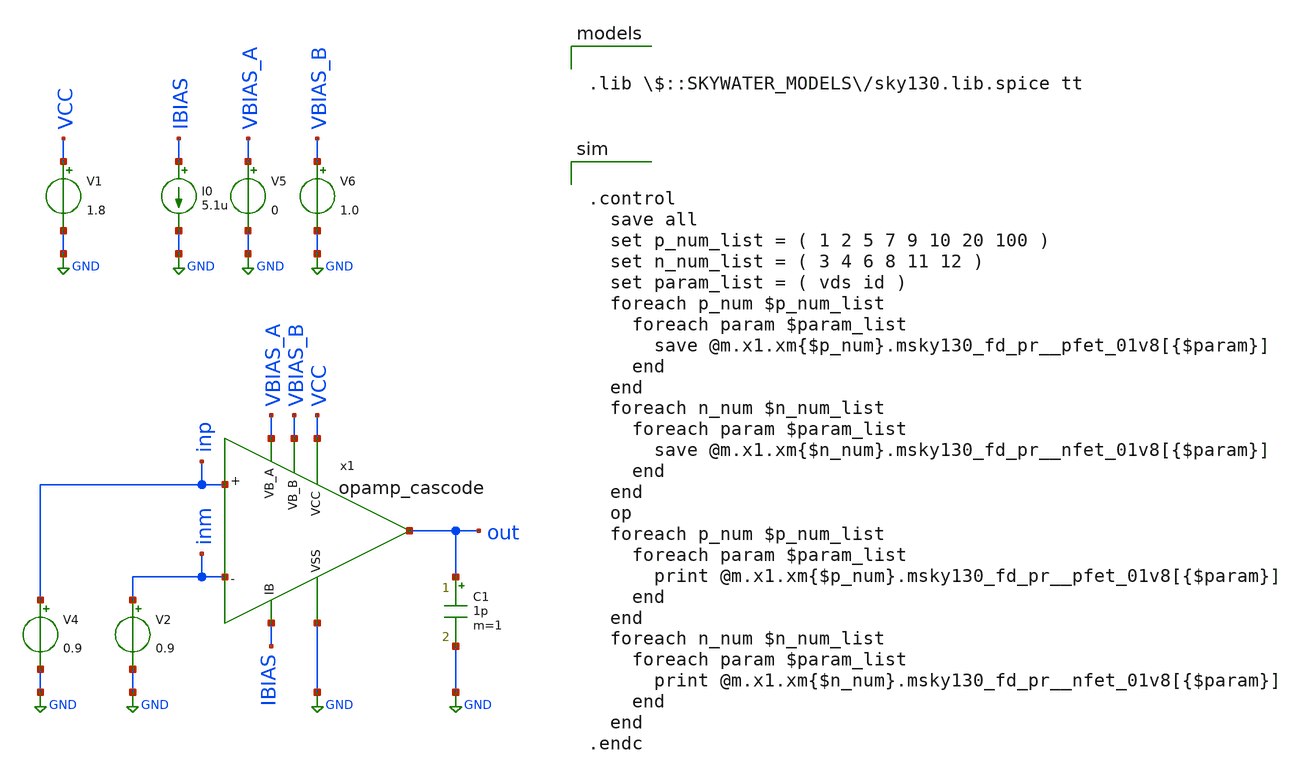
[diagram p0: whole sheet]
** sch_path: opamp_cascode_op_point.sch
**.subckt opamp_cascode_op_point
V1 VCC GND 1.8
V4 inp GND 0.9
V2 inm GND 0.9
C1 out GND 1p m=1
x1 VCC GND VBIAS_B inp inm out IBIAS VBIAS_A opamp_cascode
V5 VBIAS_A GND 0
V6 VBIAS_B GND 1.0
I0 IBIAS GND 5.1u
**** begin user architecture code


.control
  save all
  set p_num_list = ( 1 2 5 7 9 10 20 100 )
  set n_num_list = ( 3 4 6 8 11 12 )
  set param_list = ( vds id )
  foreach p_num $p_num_list
    foreach param $param_list
      save @m.x1.xm{$p_num}.msky130_fd_pr__pfet_01v8[{$param}]
    end
  end
  foreach n_num $n_num_list
    foreach param $param_list
      save @m.x1.xm{$n_num}.msky130_fd_pr__nfet_01v8[{$param}]
    end
  end
  op
  foreach p_num $p_num_list
    foreach param $param_list
      print @m.x1.xm{$p_num}.msky130_fd_pr__pfet_01v8[{$param}]
    end
  end
  foreach n_num $n_num_list
    foreach param $param_list
      print @m.x1.xm{$n_num}.msky130_fd_pr__nfet_01v8[{$param}]
    end
  end
.endc



.lib $::SKYWATER_MODELS/sky130.lib.spice tt

**** end user architecture code
**.ends

* expanding   symbol:  /home/zwierzak/projects/SKY130_OpAmp_GIT/opamp_cascode.sym # of pins=8
** sym_path: 03_Layout/opamp_cascode.sym
** sch_path: 03_Layout/opamp_cascode.sch
.subckt opamp_cascode VCC VSS VB_B IN_P IN_M OUT IB VB_A
*.ipin IN_P
*.ipin IN_M
*.ipin VCC
*.ipin VSS
*.opin OUT
*.ipin VB_A
*.ipin VB_B
*.ipin IB
XM100_3 IB IB VCC VCC sky130_fd_pr__pfet_01v8 L=3 W=5 nf=1 ad='int((nf+1)/2) * W/nf * 0.29' as='int((nf+2)/2) * W/nf * 0.29'
+ pd='2*int((nf+1)/2) * (W/nf + 0.29)' ps='2*int((nf+2)/2) * (W/nf + 0.29)' nrd='0.29 / W' nrs='0.29 / W'
+ sa=0 sb=0 sd=0 mult=2 m=2
XM10 OUT VB_A m9m10 VCC sky130_fd_pr__pfet_01v8 L=5 W=5 nf=1 ad='int((nf+1)/2) * W/nf * 0.29' as='int((nf+2)/2) * W/nf * 0.29'
+ pd='2*int((nf+1)/2) * (W/nf + 0.29)' ps='2*int((nf+2)/2) * (W/nf + 0.29)' nrd='0.29 / W' nrs='0.29 / W'
+ sa=0 sb=0 sd=0 mult=15 m=15
XM2 bias1 VB_A m1m2 VCC sky130_fd_pr__pfet_01v8 L=5 W=5 nf=1 ad='int((nf+1)/2) * W/nf * 0.29' as='int((nf+2)/2) * W/nf * 0.29'
+ pd='2*int((nf+1)/2) * (W/nf + 0.29)' ps='2*int((nf+2)/2) * (W/nf + 0.29)' nrd='0.29 / W' nrs='0.29 / W'
+ sa=0 sb=0 sd=0 mult=15 m=15
XM5 bias3 IN_M m100m5 VCC sky130_fd_pr__pfet_01v8 L=0.18 W=5 nf=1 ad='int((nf+1)/2) * W/nf * 0.29' as='int((nf+2)/2) * W/nf * 0.29'
+ pd='2*int((nf+1)/2) * (W/nf + 0.29)' ps='2*int((nf+2)/2) * (W/nf + 0.29)' nrd='0.29 / W' nrs='0.29 / W'
+ sa=0 sb=0 sd=0 mult=15 m=15
XM7 bias21 IN_P m100m5 VCC sky130_fd_pr__pfet_01v8 L=0.18 W=5 nf=1 ad='int((nf+1)/2) * W/nf * 0.29' as='int((nf+2)/2) * W/nf * 0.29'
+ pd='2*int((nf+1)/2) * (W/nf + 0.29)' ps='2*int((nf+2)/2) * (W/nf + 0.29)' nrd='0.29 / W' nrs='0.29 / W'
+ sa=0 sb=0 sd=0 mult=15 m=15
XM6 bias3 bias3 VSS VSS sky130_fd_pr__nfet_01v8 L=1 W=1.25 nf=1 ad='int((nf+1)/2) * W/nf * 0.29' as='int((nf+2)/2) * W/nf * 0.29'
+ pd='2*int((nf+1)/2) * (W/nf + 0.29)' ps='2*int((nf+2)/2) * (W/nf + 0.29)' nrd='0.29 / W' nrs='0.29 / W'
+ sa=0 sb=0 sd=0 mult=1 m=1
XM8 bias21 bias21 VSS VSS sky130_fd_pr__nfet_01v8 L=1 W=1.25 nf=1 ad='int((nf+1)/2) * W/nf * 0.29' as='int((nf+2)/2) * W/nf * 0.29'
+ pd='2*int((nf+1)/2) * (W/nf + 0.29)' ps='2*int((nf+2)/2) * (W/nf + 0.29)' nrd='0.29 / W' nrs='0.29 / W'
+ sa=0 sb=0 sd=0 mult=1 m=1
XM12 m11m12 bias21 VSS VSS sky130_fd_pr__nfet_01v8 L=1 W=5 nf=1 ad='int((nf+1)/2) * W/nf * 0.29' as='int((nf+2)/2) * W/nf * 0.29'
+ pd='2*int((nf+1)/2) * (W/nf + 0.29)' ps='2*int((nf+2)/2) * (W/nf + 0.29)' nrd='0.29 / W' nrs='0.29 / W'
+ sa=0 sb=0 sd=0 mult=1 m=1
XM11 OUT VB_B m11m12 VSS sky130_fd_pr__nfet_01v8 L=5 W=5 nf=1 ad='int((nf+1)/2) * W/nf * 0.29' as='int((nf+2)/2) * W/nf * 0.29'
+ pd='2*int((nf+1)/2) * (W/nf + 0.29)' ps='2*int((nf+2)/2) * (W/nf + 0.29)' nrd='0.29 / W' nrs='0.29 / W'
+ sa=0 sb=0 sd=0 mult=15 m=15
XM3 bias1 VB_B m3m4 VSS sky130_fd_pr__nfet_01v8 L=5 W=5 nf=1 ad='int((nf+1)/2) * W/nf * 0.29' as='int((nf+2)/2) * W/nf * 0.29'
+ pd='2*int((nf+1)/2) * (W/nf + 0.29)' ps='2*int((nf+2)/2) * (W/nf + 0.29)' nrd='0.29 / W' nrs='0.29 / W'
+ sa=0 sb=0 sd=0 mult=15 m=15
XM100_1 m100m5 IB VCC VCC sky130_fd_pr__pfet_01v8 L=3 W=5 nf=1 ad='int((nf+1)/2) * W/nf * 0.29' as='int((nf+2)/2) * W/nf * 0.29'
+ pd='2*int((nf+1)/2) * (W/nf + 0.29)' ps='2*int((nf+2)/2) * (W/nf + 0.29)' nrd='0.29 / W' nrs='0.29 / W'
+ sa=0 sb=0 sd=0 mult=3 m=3
XM5_1 bias3 IN_M m100m5 VCC sky130_fd_pr__pfet_01v8 L=0.18 W=5 nf=1 ad='int((nf+1)/2) * W/nf * 0.29'
+ as='int((nf+2)/2) * W/nf * 0.29' pd='2*int((nf+1)/2) * (W/nf + 0.29)' ps='2*int((nf+2)/2) * (W/nf + 0.29)'
+ nrd='0.29 / W' nrs='0.29 / W' sa=0 sb=0 sd=0 mult=15 m=15
XM7_1 bias21 IN_P m100m5 VCC sky130_fd_pr__pfet_01v8 L=0.18 W=5 nf=1 ad='int((nf+1)/2) * W/nf * 0.29'
+ as='int((nf+2)/2) * W/nf * 0.29' pd='2*int((nf+1)/2) * (W/nf + 0.29)' ps='2*int((nf+2)/2) * (W/nf + 0.29)'
+ nrd='0.29 / W' nrs='0.29 / W' sa=0 sb=0 sd=0 mult=15 m=15
XM9 m9m10 bias1 VCC VCC sky130_fd_pr__pfet_01v8 L=15 W=5 nf=1 ad='int((nf+1)/2) * W/nf * 0.29' as='int((nf+2)/2) * W/nf * 0.29'
+ pd='2*int((nf+1)/2) * (W/nf + 0.29)' ps='2*int((nf+2)/2) * (W/nf + 0.29)' nrd='0.29 / W' nrs='0.29 / W'
+ sa=0 sb=0 sd=0 mult=100 m=100
XM9_1 m9m10 bias1 VCC VCC sky130_fd_pr__pfet_01v8 L=15 W=5 nf=1 ad='int((nf+1)/2) * W/nf * 0.29' as='int((nf+2)/2) * W/nf * 0.29'
+ pd='2*int((nf+1)/2) * (W/nf + 0.29)' ps='2*int((nf+2)/2) * (W/nf + 0.29)' nrd='0.29 / W' nrs='0.29 / W'
+ sa=0 sb=0 sd=0 mult=100 m=100
XM9_2 m9m10 bias1 VCC VCC sky130_fd_pr__pfet_01v8 L=15 W=5 nf=1 ad='int((nf+1)/2) * W/nf * 0.29' as='int((nf+2)/2) * W/nf * 0.29'
+ pd='2*int((nf+1)/2) * (W/nf + 0.29)' ps='2*int((nf+2)/2) * (W/nf + 0.29)' nrd='0.29 / W' nrs='0.29 / W'
+ sa=0 sb=0 sd=0 mult=100 m=100
XM9_3 m9m10 bias1 VCC VCC sky130_fd_pr__pfet_01v8 L=15 W=5 nf=1 ad='int((nf+1)/2) * W/nf * 0.29' as='int((nf+2)/2) * W/nf * 0.29'
+ pd='2*int((nf+1)/2) * (W/nf + 0.29)' ps='2*int((nf+2)/2) * (W/nf + 0.29)' nrd='0.29 / W' nrs='0.29 / W'
+ sa=0 sb=0 sd=0 mult=100 m=100
XM9_4 m9m10 bias1 VCC VCC sky130_fd_pr__pfet_01v8 L=15 W=5 nf=1 ad='int((nf+1)/2) * W/nf * 0.29' as='int((nf+2)/2) * W/nf * 0.29'
+ pd='2*int((nf+1)/2) * (W/nf + 0.29)' ps='2*int((nf+2)/2) * (W/nf + 0.29)' nrd='0.29 / W' nrs='0.29 / W'
+ sa=0 sb=0 sd=0 mult=100 m=100
XM1 m1m2 bias1 VCC VCC sky130_fd_pr__pfet_01v8 L=15 W=5 nf=1 ad='int((nf+1)/2) * W/nf * 0.29' as='int((nf+2)/2) * W/nf * 0.29'
+ pd='2*int((nf+1)/2) * (W/nf + 0.29)' ps='2*int((nf+2)/2) * (W/nf + 0.29)' nrd='0.29 / W' nrs='0.29 / W'
+ sa=0 sb=0 sd=0 mult=100 m=100
XM1_1 m1m2 bias1 VCC VCC sky130_fd_pr__pfet_01v8 L=15 W=5 nf=1 ad='int((nf+1)/2) * W/nf * 0.29' as='int((nf+2)/2) * W/nf * 0.29'
+ pd='2*int((nf+1)/2) * (W/nf + 0.29)' ps='2*int((nf+2)/2) * (W/nf + 0.29)' nrd='0.29 / W' nrs='0.29 / W'
+ sa=0 sb=0 sd=0 mult=100 m=100
XM1_2 m1m2 bias1 VCC VCC sky130_fd_pr__pfet_01v8 L=15 W=5 nf=1 ad='int((nf+1)/2) * W/nf * 0.29' as='int((nf+2)/2) * W/nf * 0.29'
+ pd='2*int((nf+1)/2) * (W/nf + 0.29)' ps='2*int((nf+2)/2) * (W/nf + 0.29)' nrd='0.29 / W' nrs='0.29 / W'
+ sa=0 sb=0 sd=0 mult=100 m=100
XM1_3 m1m2 bias1 VCC VCC sky130_fd_pr__pfet_01v8 L=15 W=5 nf=1 ad='int((nf+1)/2) * W/nf * 0.29' as='int((nf+2)/2) * W/nf * 0.29'
+ pd='2*int((nf+1)/2) * (W/nf + 0.29)' ps='2*int((nf+2)/2) * (W/nf + 0.29)' nrd='0.29 / W' nrs='0.29 / W'
+ sa=0 sb=0 sd=0 mult=100 m=100
XM1_4 m1m2 bias1 VCC VCC sky130_fd_pr__pfet_01v8 L=15 W=5 nf=1 ad='int((nf+1)/2) * W/nf * 0.29' as='int((nf+2)/2) * W/nf * 0.29'
+ pd='2*int((nf+1)/2) * (W/nf + 0.29)' ps='2*int((nf+2)/2) * (W/nf + 0.29)' nrd='0.29 / W' nrs='0.29 / W'
+ sa=0 sb=0 sd=0 mult=100 m=100
XM100_2 m100m5 IB VCC VCC sky130_fd_pr__pfet_01v8 L=3 W=5 nf=1 ad='int((nf+1)/2) * W/nf * 0.29' as='int((nf+2)/2) * W/nf * 0.29'
+ pd='2*int((nf+1)/2) * (W/nf + 0.29)' ps='2*int((nf+2)/2) * (W/nf + 0.29)' nrd='0.29 / W' nrs='0.29 / W'
+ sa=0 sb=0 sd=0 mult=3 m=3
XM10_1 OUT VB_A m9m10 VCC sky130_fd_pr__pfet_01v8 L=5 W=5 nf=1 ad='int((nf+1)/2) * W/nf * 0.29' as='int((nf+2)/2) * W/nf * 0.29'
+ pd='2*int((nf+1)/2) * (W/nf + 0.29)' ps='2*int((nf+2)/2) * (W/nf + 0.29)' nrd='0.29 / W' nrs='0.29 / W'
+ sa=0 sb=0 sd=0 mult=15 m=15
XM2_1 bias1 VB_A m1m2 VCC sky130_fd_pr__pfet_01v8 L=5 W=5 nf=1 ad='int((nf+1)/2) * W/nf * 0.29' as='int((nf+2)/2) * W/nf * 0.29'
+ pd='2*int((nf+1)/2) * (W/nf + 0.29)' ps='2*int((nf+2)/2) * (W/nf + 0.29)' nrd='0.29 / W' nrs='0.29 / W'
+ sa=0 sb=0 sd=0 mult=15 m=15
XM3_1 bias1 VB_B m3m4 VSS sky130_fd_pr__nfet_01v8 L=5 W=5 nf=1 ad='int((nf+1)/2) * W/nf * 0.29' as='int((nf+2)/2) * W/nf * 0.29'
+ pd='2*int((nf+1)/2) * (W/nf + 0.29)' ps='2*int((nf+2)/2) * (W/nf + 0.29)' nrd='0.29 / W' nrs='0.29 / W'
+ sa=0 sb=0 sd=0 mult=15 m=15
XM11_1 OUT VB_B m11m12 VSS sky130_fd_pr__nfet_01v8 L=5 W=5 nf=1 ad='int((nf+1)/2) * W/nf * 0.29' as='int((nf+2)/2) * W/nf * 0.29'
+ pd='2*int((nf+1)/2) * (W/nf + 0.29)' ps='2*int((nf+2)/2) * (W/nf + 0.29)' nrd='0.29 / W' nrs='0.29 / W'
+ sa=0 sb=0 sd=0 mult=15 m=15
XM4 m3m4 bias3 VSS VSS sky130_fd_pr__nfet_01v8 L=1 W=5 nf=1 ad='int((nf+1)/2) * W/nf * 0.29' as='int((nf+2)/2) * W/nf * 0.29'
+ pd='2*int((nf+1)/2) * (W/nf + 0.29)' ps='2*int((nf+2)/2) * (W/nf + 0.29)' nrd='0.29 / W' nrs='0.29 / W'
+ sa=0 sb=0 sd=0 mult=1 m=1
XM6_1 bias3 bias3 VSS VSS sky130_fd_pr__nfet_01v8 L=1 W=1.25 nf=1 ad='int((nf+1)/2) * W/nf * 0.29' as='int((nf+2)/2) * W/nf * 0.29'
+ pd='2*int((nf+1)/2) * (W/nf + 0.29)' ps='2*int((nf+2)/2) * (W/nf + 0.29)' nrd='0.29 / W' nrs='0.29 / W'
+ sa=0 sb=0 sd=0 mult=1 m=1
XM8_1 bias21 bias21 VSS VSS sky130_fd_pr__nfet_01v8 L=1 W=1.25 nf=1 ad='int((nf+1)/2) * W/nf * 0.29'
+ as='int((nf+2)/2) * W/nf * 0.29' pd='2*int((nf+1)/2) * (W/nf + 0.29)' ps='2*int((nf+2)/2) * (W/nf + 0.29)'
+ nrd='0.29 / W' nrs='0.29 / W' sa=0 sb=0 sd=0 mult=1 m=1
XM6_2 bias3 bias3 VSS VSS sky130_fd_pr__nfet_01v8 L=1 W=1.25 nf=1 ad='int((nf+1)/2) * W/nf * 0.29' as='int((nf+2)/2) * W/nf * 0.29'
+ pd='2*int((nf+1)/2) * (W/nf + 0.29)' ps='2*int((nf+2)/2) * (W/nf + 0.29)' nrd='0.29 / W' nrs='0.29 / W'
+ sa=0 sb=0 sd=0 mult=1 m=1
XM6_3 bias3 bias3 VSS VSS sky130_fd_pr__nfet_01v8 L=1 W=1.25 nf=1 ad='int((nf+1)/2) * W/nf * 0.29' as='int((nf+2)/2) * W/nf * 0.29'
+ pd='2*int((nf+1)/2) * (W/nf + 0.29)' ps='2*int((nf+2)/2) * (W/nf + 0.29)' nrd='0.29 / W' nrs='0.29 / W'
+ sa=0 sb=0 sd=0 mult=1 m=1
XM9_dummy_1 dummy_9 bias1 dummy_9 VCC sky130_fd_pr__pfet_01v8 L=15 W=5 nf=1 ad='int((nf+1)/2) * W/nf * 0.29'
+ as='int((nf+2)/2) * W/nf * 0.29' pd='2*int((nf+1)/2) * (W/nf + 0.29)' ps='2*int((nf+2)/2) * (W/nf + 0.29)'
+ nrd='0.29 / W' nrs='0.29 / W' sa=0 sb=0 sd=0 mult=102 m=102
XM9_dummy_2 dummy_9 bias1 dummy_9 VCC sky130_fd_pr__pfet_01v8 L=15 W=5 nf=1 ad='int((nf+1)/2) * W/nf * 0.29'
+ as='int((nf+2)/2) * W/nf * 0.29' pd='2*int((nf+1)/2) * (W/nf + 0.29)' ps='2*int((nf+2)/2) * (W/nf + 0.29)'
+ nrd='0.29 / W' nrs='0.29 / W' sa=0 sb=0 sd=0 mult=102 m=102
XM9_dummy_3 dummy_9 bias1 dummy_9 VCC sky130_fd_pr__pfet_01v8 L=15 W=5 nf=1 ad='int((nf+1)/2) * W/nf * 0.29'
+ as='int((nf+2)/2) * W/nf * 0.29' pd='2*int((nf+1)/2) * (W/nf + 0.29)' ps='2*int((nf+2)/2) * (W/nf + 0.29)'
+ nrd='0.29 / W' nrs='0.29 / W' sa=0 sb=0 sd=0 mult=1 m=1
XM9_dummy_4 dummy_9 bias1 dummy_9 VCC sky130_fd_pr__pfet_01v8 L=15 W=5 nf=1 ad='int((nf+1)/2) * W/nf * 0.29'
+ as='int((nf+2)/2) * W/nf * 0.29' pd='2*int((nf+1)/2) * (W/nf + 0.29)' ps='2*int((nf+2)/2) * (W/nf + 0.29)'
+ nrd='0.29 / W' nrs='0.29 / W' sa=0 sb=0 sd=0 mult=1 m=1
XM9_dummy_5 dummy_9 bias1 dummy_9 VCC sky130_fd_pr__pfet_01v8 L=15 W=5 nf=1 ad='int((nf+1)/2) * W/nf * 0.29'
+ as='int((nf+2)/2) * W/nf * 0.29' pd='2*int((nf+1)/2) * (W/nf + 0.29)' ps='2*int((nf+2)/2) * (W/nf + 0.29)'
+ nrd='0.29 / W' nrs='0.29 / W' sa=0 sb=0 sd=0 mult=1 m=1
XM9_dummy_6 dummy_9 bias1 dummy_9 VCC sky130_fd_pr__pfet_01v8 L=15 W=5 nf=1 ad='int((nf+1)/2) * W/nf * 0.29'
+ as='int((nf+2)/2) * W/nf * 0.29' pd='2*int((nf+1)/2) * (W/nf + 0.29)' ps='2*int((nf+2)/2) * (W/nf + 0.29)'
+ nrd='0.29 / W' nrs='0.29 / W' sa=0 sb=0 sd=0 mult=1 m=1
XM9_dummy_7 dummy_9 bias1 dummy_9 VCC sky130_fd_pr__pfet_01v8 L=15 W=5 nf=1 ad='int((nf+1)/2) * W/nf * 0.29'
+ as='int((nf+2)/2) * W/nf * 0.29' pd='2*int((nf+1)/2) * (W/nf + 0.29)' ps='2*int((nf+2)/2) * (W/nf + 0.29)'
+ nrd='0.29 / W' nrs='0.29 / W' sa=0 sb=0 sd=0 mult=1 m=1
XM9_dummy_8 dummy_9 bias1 dummy_9 VCC sky130_fd_pr__pfet_01v8 L=15 W=5 nf=1 ad='int((nf+1)/2) * W/nf * 0.29'
+ as='int((nf+2)/2) * W/nf * 0.29' pd='2*int((nf+1)/2) * (W/nf + 0.29)' ps='2*int((nf+2)/2) * (W/nf + 0.29)'
+ nrd='0.29 / W' nrs='0.29 / W' sa=0 sb=0 sd=0 mult=1 m=1
XM9_dummy_9 dummy_9 bias1 dummy_9 VCC sky130_fd_pr__pfet_01v8 L=15 W=5 nf=1 ad='int((nf+1)/2) * W/nf * 0.29'
+ as='int((nf+2)/2) * W/nf * 0.29' pd='2*int((nf+1)/2) * (W/nf + 0.29)' ps='2*int((nf+2)/2) * (W/nf + 0.29)'
+ nrd='0.29 / W' nrs='0.29 / W' sa=0 sb=0 sd=0 mult=1 m=1
XM9_dummy_10 dummy_9 bias1 dummy_9 VCC sky130_fd_pr__pfet_01v8 L=15 W=5 nf=1 ad='int((nf+1)/2) * W/nf * 0.29'
+ as='int((nf+2)/2) * W/nf * 0.29' pd='2*int((nf+1)/2) * (W/nf + 0.29)' ps='2*int((nf+2)/2) * (W/nf + 0.29)'
+ nrd='0.29 / W' nrs='0.29 / W' sa=0 sb=0 sd=0 mult=1 m=1
XM9_dummy_11 dummy_9 bias1 dummy_9 VCC sky130_fd_pr__pfet_01v8 L=15 W=5 nf=1 ad='int((nf+1)/2) * W/nf * 0.29'
+ as='int((nf+2)/2) * W/nf * 0.29' pd='2*int((nf+1)/2) * (W/nf + 0.29)' ps='2*int((nf+2)/2) * (W/nf + 0.29)'
+ nrd='0.29 / W' nrs='0.29 / W' sa=0 sb=0 sd=0 mult=1 m=1
XM9_dummy_12 dummy_9 bias1 dummy_9 VCC sky130_fd_pr__pfet_01v8 L=15 W=5 nf=1 ad='int((nf+1)/2) * W/nf * 0.29'
+ as='int((nf+2)/2) * W/nf * 0.29' pd='2*int((nf+1)/2) * (W/nf + 0.29)' ps='2*int((nf+2)/2) * (W/nf + 0.29)'
+ nrd='0.29 / W' nrs='0.29 / W' sa=0 sb=0 sd=0 mult=1 m=1
XM100_dummy_1 dummy_100 IB dummy_100 VCC sky130_fd_pr__pfet_01v8 L=3 W=5 nf=1 ad='int((nf+1)/2) * W/nf * 0.29'
+ as='int((nf+2)/2) * W/nf * 0.29' pd='2*int((nf+1)/2) * (W/nf + 0.29)' ps='2*int((nf+2)/2) * (W/nf + 0.29)'
+ nrd='0.29 / W' nrs='0.29 / W' sa=0 sb=0 sd=0 mult=5 m=5
XM100_dummy_2 dummy_100 IB dummy_100 VCC sky130_fd_pr__pfet_01v8 L=3 W=5 nf=1 ad='int((nf+1)/2) * W/nf * 0.29'
+ as='int((nf+2)/2) * W/nf * 0.29' pd='2*int((nf+1)/2) * (W/nf + 0.29)' ps='2*int((nf+2)/2) * (W/nf + 0.29)'
+ nrd='0.29 / W' nrs='0.29 / W' sa=0 sb=0 sd=0 mult=5 m=5
XM100_dummy_3 dummy_100 IB dummy_100 VCC sky130_fd_pr__pfet_01v8 L=3 W=5 nf=1 ad='int((nf+1)/2) * W/nf * 0.29'
+ as='int((nf+2)/2) * W/nf * 0.29' pd='2*int((nf+1)/2) * (W/nf + 0.29)' ps='2*int((nf+2)/2) * (W/nf + 0.29)'
+ nrd='0.29 / W' nrs='0.29 / W' sa=0 sb=0 sd=0 mult=2 m=2
XM100_dummy_4 dummy_100 IB dummy_100 VCC sky130_fd_pr__pfet_01v8 L=3 W=5 nf=1 ad='int((nf+1)/2) * W/nf * 0.29'
+ as='int((nf+2)/2) * W/nf * 0.29' pd='2*int((nf+1)/2) * (W/nf + 0.29)' ps='2*int((nf+2)/2) * (W/nf + 0.29)'
+ nrd='0.29 / W' nrs='0.29 / W' sa=0 sb=0 sd=0 mult=2 m=2
XM100_dummy_5 dummy_100 IB dummy_100 VCC sky130_fd_pr__pfet_01v8 L=3 W=5 nf=1 ad='int((nf+1)/2) * W/nf * 0.29'
+ as='int((nf+2)/2) * W/nf * 0.29' pd='2*int((nf+1)/2) * (W/nf + 0.29)' ps='2*int((nf+2)/2) * (W/nf + 0.29)'
+ nrd='0.29 / W' nrs='0.29 / W' sa=0 sb=0 sd=0 mult=1 m=1
XM100_dummy_6 dummy_100 IB dummy_100 VCC sky130_fd_pr__pfet_01v8 L=3 W=5 nf=1 ad='int((nf+1)/2) * W/nf * 0.29'
+ as='int((nf+2)/2) * W/nf * 0.29' pd='2*int((nf+1)/2) * (W/nf + 0.29)' ps='2*int((nf+2)/2) * (W/nf + 0.29)'
+ nrd='0.29 / W' nrs='0.29 / W' sa=0 sb=0 sd=0 mult=1 m=1
XM100_dummy_7 dummy_100 IB dummy_100 VCC sky130_fd_pr__pfet_01v8 L=3 W=5 nf=1 ad='int((nf+1)/2) * W/nf * 0.29'
+ as='int((nf+2)/2) * W/nf * 0.29' pd='2*int((nf+1)/2) * (W/nf + 0.29)' ps='2*int((nf+2)/2) * (W/nf + 0.29)'
+ nrd='0.29 / W' nrs='0.29 / W' sa=0 sb=0 sd=0 mult=1 m=1
XM100_dummy_8 dummy_100 IB dummy_100 VCC sky130_fd_pr__pfet_01v8 L=3 W=5 nf=1 ad='int((nf+1)/2) * W/nf * 0.29'
+ as='int((nf+2)/2) * W/nf * 0.29' pd='2*int((nf+1)/2) * (W/nf + 0.29)' ps='2*int((nf+2)/2) * (W/nf + 0.29)'
+ nrd='0.29 / W' nrs='0.29 / W' sa=0 sb=0 sd=0 mult=1 m=1
XM100_dummy_9 dummy_100 IB dummy_100 VCC sky130_fd_pr__pfet_01v8 L=3 W=5 nf=1 ad='int((nf+1)/2) * W/nf * 0.29'
+ as='int((nf+2)/2) * W/nf * 0.29' pd='2*int((nf+1)/2) * (W/nf + 0.29)' ps='2*int((nf+2)/2) * (W/nf + 0.29)'
+ nrd='0.29 / W' nrs='0.29 / W' sa=0 sb=0 sd=0 mult=1 m=1
XM100_dummy_10 dummy_100 IB dummy_100 VCC sky130_fd_pr__pfet_01v8 L=3 W=5 nf=1 ad='int((nf+1)/2) * W/nf * 0.29'
+ as='int((nf+2)/2) * W/nf * 0.29' pd='2*int((nf+1)/2) * (W/nf + 0.29)' ps='2*int((nf+2)/2) * (W/nf + 0.29)'
+ nrd='0.29 / W' nrs='0.29 / W' sa=0 sb=0 sd=0 mult=1 m=1
XM2_dummy_1 dummy_2 VB_A dummy_2 VCC sky130_fd_pr__pfet_01v8 L=5 W=5 nf=1 ad='int((nf+1)/2) * W/nf * 0.29'
+ as='int((nf+2)/2) * W/nf * 0.29' pd='2*int((nf+1)/2) * (W/nf + 0.29)' ps='2*int((nf+2)/2) * (W/nf + 0.29)'
+ nrd='0.29 / W' nrs='0.29 / W' sa=0 sb=0 sd=0 mult=17 m=17
XM2_dummy_2 dummy_2 VB_A dummy_2 VCC sky130_fd_pr__pfet_01v8 L=5 W=5 nf=1 ad='int((nf+1)/2) * W/nf * 0.29'
+ as='int((nf+2)/2) * W/nf * 0.29' pd='2*int((nf+1)/2) * (W/nf + 0.29)' ps='2*int((nf+2)/2) * (W/nf + 0.29)'
+ nrd='0.29 / W' nrs='0.29 / W' sa=0 sb=0 sd=0 mult=17 m=17
XM2_dummy_3 dummy_2 VB_A dummy_2 VCC sky130_fd_pr__pfet_01v8 L=5 W=5 nf=1 ad='int((nf+1)/2) * W/nf * 0.29'
+ as='int((nf+2)/2) * W/nf * 0.29' pd='2*int((nf+1)/2) * (W/nf + 0.29)' ps='2*int((nf+2)/2) * (W/nf + 0.29)'
+ nrd='0.29 / W' nrs='0.29 / W' sa=0 sb=0 sd=0 mult=1 m=1
XM2_dummy_4 dummy_2 VB_A dummy_2 VCC sky130_fd_pr__pfet_01v8 L=5 W=5 nf=1 ad='int((nf+1)/2) * W/nf * 0.29'
+ as='int((nf+2)/2) * W/nf * 0.29' pd='2*int((nf+1)/2) * (W/nf + 0.29)' ps='2*int((nf+2)/2) * (W/nf + 0.29)'
+ nrd='0.29 / W' nrs='0.29 / W' sa=0 sb=0 sd=0 mult=1 m=1
XM2_dummy_5 dummy_2 VB_A dummy_2 VCC sky130_fd_pr__pfet_01v8 L=5 W=5 nf=1 ad='int((nf+1)/2) * W/nf * 0.29'
+ as='int((nf+2)/2) * W/nf * 0.29' pd='2*int((nf+1)/2) * (W/nf + 0.29)' ps='2*int((nf+2)/2) * (W/nf + 0.29)'
+ nrd='0.29 / W' nrs='0.29 / W' sa=0 sb=0 sd=0 mult=1 m=1
XM2_dummy_6 dummy_2 VB_A dummy_2 VCC sky130_fd_pr__pfet_01v8 L=5 W=5 nf=1 ad='int((nf+1)/2) * W/nf * 0.29'
+ as='int((nf+2)/2) * W/nf * 0.29' pd='2*int((nf+1)/2) * (W/nf + 0.29)' ps='2*int((nf+2)/2) * (W/nf + 0.29)'
+ nrd='0.29 / W' nrs='0.29 / W' sa=0 sb=0 sd=0 mult=1 m=1
XM2_dummy_7 dummy_2 VB_A dummy_2 VCC sky130_fd_pr__pfet_01v8 L=5 W=5 nf=1 ad='int((nf+1)/2) * W/nf * 0.29'
+ as='int((nf+2)/2) * W/nf * 0.29' pd='2*int((nf+1)/2) * (W/nf + 0.29)' ps='2*int((nf+2)/2) * (W/nf + 0.29)'
+ nrd='0.29 / W' nrs='0.29 / W' sa=0 sb=0 sd=0 mult=1 m=1
XM2_dummy_8 dummy_2 VB_A dummy_2 VCC sky130_fd_pr__pfet_01v8 L=5 W=5 nf=1 ad='int((nf+1)/2) * W/nf * 0.29'
+ as='int((nf+2)/2) * W/nf * 0.29' pd='2*int((nf+1)/2) * (W/nf + 0.29)' ps='2*int((nf+2)/2) * (W/nf + 0.29)'
+ nrd='0.29 / W' nrs='0.29 / W' sa=0 sb=0 sd=0 mult=1 m=1
XM2_dummy_9 dummy_2 VB_A dummy_2 VCC sky130_fd_pr__pfet_01v8 L=5 W=5 nf=1 ad='int((nf+1)/2) * W/nf * 0.29'
+ as='int((nf+2)/2) * W/nf * 0.29' pd='2*int((nf+1)/2) * (W/nf + 0.29)' ps='2*int((nf+2)/2) * (W/nf + 0.29)'
+ nrd='0.29 / W' nrs='0.29 / W' sa=0 sb=0 sd=0 mult=1 m=1
XM2_dummy_10 dummy_2 VB_A dummy_2 VCC sky130_fd_pr__pfet_01v8 L=5 W=5 nf=1 ad='int((nf+1)/2) * W/nf * 0.29'
+ as='int((nf+2)/2) * W/nf * 0.29' pd='2*int((nf+1)/2) * (W/nf + 0.29)' ps='2*int((nf+2)/2) * (W/nf + 0.29)'
+ nrd='0.29 / W' nrs='0.29 / W' sa=0 sb=0 sd=0 mult=1 m=1
XM4_dummy_1 dummy_4 bias3 dummy_4 VSS sky130_fd_pr__nfet_01v8 L=1 W=1.25 nf=1 ad='int((nf+1)/2) * W/nf * 0.29'
+ as='int((nf+2)/2) * W/nf * 0.29' pd='2*int((nf+1)/2) * (W/nf + 0.29)' ps='2*int((nf+2)/2) * (W/nf + 0.29)'
+ nrd='0.29 / W' nrs='0.29 / W' sa=0 sb=0 sd=0 mult=6 m=6
XM4_dummy_2 dummy_4 bias3 dummy_4 VSS sky130_fd_pr__nfet_01v8 L=1 W=1.25 nf=1 ad='int((nf+1)/2) * W/nf * 0.29'
+ as='int((nf+2)/2) * W/nf * 0.29' pd='2*int((nf+1)/2) * (W/nf + 0.29)' ps='2*int((nf+2)/2) * (W/nf + 0.29)'
+ nrd='0.29 / W' nrs='0.29 / W' sa=0 sb=0 sd=0 mult=6 m=6
XM4_dummy_3 dummy_4 bias3 dummy_4 VSS sky130_fd_pr__nfet_01v8 L=1 W=1.25 nf=1 ad='int((nf+1)/2) * W/nf * 0.29'
+ as='int((nf+2)/2) * W/nf * 0.29' pd='2*int((nf+1)/2) * (W/nf + 0.29)' ps='2*int((nf+2)/2) * (W/nf + 0.29)'
+ nrd='0.29 / W' nrs='0.29 / W' sa=0 sb=0 sd=0 mult=1 m=1
XM4_dummy_4 dummy_4 bias3 dummy_4 VSS sky130_fd_pr__nfet_01v8 L=1 W=1.25 nf=1 ad='int((nf+1)/2) * W/nf * 0.29'
+ as='int((nf+2)/2) * W/nf * 0.29' pd='2*int((nf+1)/2) * (W/nf + 0.29)' ps='2*int((nf+2)/2) * (W/nf + 0.29)'
+ nrd='0.29 / W' nrs='0.29 / W' sa=0 sb=0 sd=0 mult=1 m=1
XM4_dummy_5 dummy_4 bias3 dummy_4 VSS sky130_fd_pr__nfet_01v8 L=1 W=1.25 nf=1 ad='int((nf+1)/2) * W/nf * 0.29'
+ as='int((nf+2)/2) * W/nf * 0.29' pd='2*int((nf+1)/2) * (W/nf + 0.29)' ps='2*int((nf+2)/2) * (W/nf + 0.29)'
+ nrd='0.29 / W' nrs='0.29 / W' sa=0 sb=0 sd=0 mult=1 m=1
XM4_dummy_6 dummy_4 bias3 dummy_4 VSS sky130_fd_pr__nfet_01v8 L=1 W=1.25 nf=1 ad='int((nf+1)/2) * W/nf * 0.29'
+ as='int((nf+2)/2) * W/nf * 0.29' pd='2*int((nf+1)/2) * (W/nf + 0.29)' ps='2*int((nf+2)/2) * (W/nf + 0.29)'
+ nrd='0.29 / W' nrs='0.29 / W' sa=0 sb=0 sd=0 mult=1 m=1
XM4_dummy_7 dummy_4 bias3 dummy_4 VSS sky130_fd_pr__nfet_01v8 L=1 W=1.25 nf=1 ad='int((nf+1)/2) * W/nf * 0.29'
+ as='int((nf+2)/2) * W/nf * 0.29' pd='2*int((nf+1)/2) * (W/nf + 0.29)' ps='2*int((nf+2)/2) * (W/nf + 0.29)'
+ nrd='0.29 / W' nrs='0.29 / W' sa=0 sb=0 sd=0 mult=1 m=1
XM4_dummy_8 dummy_4 bias3 dummy_4 VSS sky130_fd_pr__nfet_01v8 L=1 W=1.25 nf=1 ad='int((nf+1)/2) * W/nf * 0.29'
+ as='int((nf+2)/2) * W/nf * 0.29' pd='2*int((nf+1)/2) * (W/nf + 0.29)' ps='2*int((nf+2)/2) * (W/nf + 0.29)'
+ nrd='0.29 / W' nrs='0.29 / W' sa=0 sb=0 sd=0 mult=1 m=1
XM4_dummy_9 dummy_4 bias3 dummy_4 VSS sky130_fd_pr__nfet_01v8 L=1 W=1.25 nf=1 ad='int((nf+1)/2) * W/nf * 0.29'
+ as='int((nf+2)/2) * W/nf * 0.29' pd='2*int((nf+1)/2) * (W/nf + 0.29)' ps='2*int((nf+2)/2) * (W/nf + 0.29)'
+ nrd='0.29 / W' nrs='0.29 / W' sa=0 sb=0 sd=0 mult=1 m=1
XM4_dummy_10 dummy_4 bias3 dummy_4 VSS sky130_fd_pr__nfet_01v8 L=1 W=1.25 nf=1 ad='int((nf+1)/2) * W/nf * 0.29'
+ as='int((nf+2)/2) * W/nf * 0.29' pd='2*int((nf+1)/2) * (W/nf + 0.29)' ps='2*int((nf+2)/2) * (W/nf + 0.29)'
+ nrd='0.29 / W' nrs='0.29 / W' sa=0 sb=0 sd=0 mult=1 m=1
XM8_2 bias21 bias21 VSS VSS sky130_fd_pr__nfet_01v8 L=1 W=1.25 nf=1 ad='int((nf+1)/2) * W/nf * 0.29'
+ as='int((nf+2)/2) * W/nf * 0.29' pd='2*int((nf+1)/2) * (W/nf + 0.29)' ps='2*int((nf+2)/2) * (W/nf + 0.29)'
+ nrd='0.29 / W' nrs='0.29 / W' sa=0 sb=0 sd=0 mult=1 m=1
XM8_3 bias21 bias21 VSS VSS sky130_fd_pr__nfet_01v8 L=1 W=1.25 nf=1 ad='int((nf+1)/2) * W/nf * 0.29'
+ as='int((nf+2)/2) * W/nf * 0.29' pd='2*int((nf+1)/2) * (W/nf + 0.29)' ps='2*int((nf+2)/2) * (W/nf + 0.29)'
+ nrd='0.29 / W' nrs='0.29 / W' sa=0 sb=0 sd=0 mult=1 m=1
XM100_4 IB IB VCC VCC sky130_fd_pr__pfet_01v8 L=3 W=5 nf=1 ad='int((nf+1)/2) * W/nf * 0.29' as='int((nf+2)/2) * W/nf * 0.29'
+ pd='2*int((nf+1)/2) * (W/nf + 0.29)' ps='2*int((nf+2)/2) * (W/nf + 0.29)' nrd='0.29 / W' nrs='0.29 / W'
+ sa=0 sb=0 sd=0 mult=2 m=2
XM3_dummy_1 dummy_3 VB_B dummy_3 VSS sky130_fd_pr__nfet_01v8 L=5 W=5 nf=1 ad='int((nf+1)/2) * W/nf * 0.29'
+ as='int((nf+2)/2) * W/nf * 0.29' pd='2*int((nf+1)/2) * (W/nf + 0.29)' ps='2*int((nf+2)/2) * (W/nf + 0.29)'
+ nrd='0.29 / W' nrs='0.29 / W' sa=0 sb=0 sd=0 mult=17 m=17
XM3_dummy_2 dummy_3 VB_B dummy_3 VSS sky130_fd_pr__nfet_01v8 L=5 W=5 nf=1 ad='int((nf+1)/2) * W/nf * 0.29'
+ as='int((nf+2)/2) * W/nf * 0.29' pd='2*int((nf+1)/2) * (W/nf + 0.29)' ps='2*int((nf+2)/2) * (W/nf + 0.29)'
+ nrd='0.29 / W' nrs='0.29 / W' sa=0 sb=0 sd=0 mult=17 m=17
XM3_dummy_3 dummy_3 VB_B dummy_3 VSS sky130_fd_pr__nfet_01v8 L=5 W=5 nf=1 ad='int((nf+1)/2) * W/nf * 0.29'
+ as='int((nf+2)/2) * W/nf * 0.29' pd='2*int((nf+1)/2) * (W/nf + 0.29)' ps='2*int((nf+2)/2) * (W/nf + 0.29)'
+ nrd='0.29 / W' nrs='0.29 / W' sa=0 sb=0 sd=0 mult=1 m=1
XM3_dummy_4 dummy_3 VB_B dummy_3 VSS sky130_fd_pr__nfet_01v8 L=5 W=5 nf=1 ad='int((nf+1)/2) * W/nf * 0.29'
+ as='int((nf+2)/2) * W/nf * 0.29' pd='2*int((nf+1)/2) * (W/nf + 0.29)' ps='2*int((nf+2)/2) * (W/nf + 0.29)'
+ nrd='0.29 / W' nrs='0.29 / W' sa=0 sb=0 sd=0 mult=1 m=1
XM3_dummy_5 dummy_3 VB_B dummy_3 VSS sky130_fd_pr__nfet_01v8 L=5 W=5 nf=1 ad='int((nf+1)/2) * W/nf * 0.29'
+ as='int((nf+2)/2) * W/nf * 0.29' pd='2*int((nf+1)/2) * (W/nf + 0.29)' ps='2*int((nf+2)/2) * (W/nf + 0.29)'
+ nrd='0.29 / W' nrs='0.29 / W' sa=0 sb=0 sd=0 mult=1 m=1
XM3_dummy_6 dummy_3 VB_B dummy_3 VSS sky130_fd_pr__nfet_01v8 L=5 W=5 nf=1 ad='int((nf+1)/2) * W/nf * 0.29'
+ as='int((nf+2)/2) * W/nf * 0.29' pd='2*int((nf+1)/2) * (W/nf + 0.29)' ps='2*int((nf+2)/2) * (W/nf + 0.29)'
+ nrd='0.29 / W' nrs='0.29 / W' sa=0 sb=0 sd=0 mult=1 m=1
XM3_dummy_7 dummy_3 VB_B dummy_3 VSS sky130_fd_pr__nfet_01v8 L=5 W=5 nf=1 ad='int((nf+1)/2) * W/nf * 0.29'
+ as='int((nf+2)/2) * W/nf * 0.29' pd='2*int((nf+1)/2) * (W/nf + 0.29)' ps='2*int((nf+2)/2) * (W/nf + 0.29)'
+ nrd='0.29 / W' nrs='0.29 / W' sa=0 sb=0 sd=0 mult=1 m=1
XM3_dummy_8 dummy_3 VB_B dummy_3 VSS sky130_fd_pr__nfet_01v8 L=5 W=5 nf=1 ad='int((nf+1)/2) * W/nf * 0.29'
+ as='int((nf+2)/2) * W/nf * 0.29' pd='2*int((nf+1)/2) * (W/nf + 0.29)' ps='2*int((nf+2)/2) * (W/nf + 0.29)'
+ nrd='0.29 / W' nrs='0.29 / W' sa=0 sb=0 sd=0 mult=1 m=1
XM3_dummy_9 dummy_3 VB_B dummy_3 VSS sky130_fd_pr__nfet_01v8 L=5 W=5 nf=1 ad='int((nf+1)/2) * W/nf * 0.29'
+ as='int((nf+2)/2) * W/nf * 0.29' pd='2*int((nf+1)/2) * (W/nf + 0.29)' ps='2*int((nf+2)/2) * (W/nf + 0.29)'
+ nrd='0.29 / W' nrs='0.29 / W' sa=0 sb=0 sd=0 mult=1 m=1
XM3_dummy_10 dummy_3 VB_B dummy_3 VSS sky130_fd_pr__nfet_01v8 L=5 W=5 nf=1 ad='int((nf+1)/2) * W/nf * 0.29'
+ as='int((nf+2)/2) * W/nf * 0.29' pd='2*int((nf+1)/2) * (W/nf + 0.29)' ps='2*int((nf+2)/2) * (W/nf + 0.29)'
+ nrd='0.29 / W' nrs='0.29 / W' sa=0 sb=0 sd=0 mult=1 m=1
XM9_dummy_13 dummy_9 bias1 dummy_9 VCC sky130_fd_pr__pfet_01v8 L=15 W=5 nf=1 ad='int((nf+1)/2) * W/nf * 0.29'
+ as='int((nf+2)/2) * W/nf * 0.29' pd='2*int((nf+1)/2) * (W/nf + 0.29)' ps='2*int((nf+2)/2) * (W/nf + 0.29)'
+ nrd='0.29 / W' nrs='0.29 / W' sa=0 sb=0 sd=0 mult=1 m=1
XM9_dummy_14 dummy_9 bias1 dummy_9 VCC sky130_fd_pr__pfet_01v8 L=15 W=5 nf=1 ad='int((nf+1)/2) * W/nf * 0.29'
+ as='int((nf+2)/2) * W/nf * 0.29' pd='2*int((nf+1)/2) * (W/nf + 0.29)' ps='2*int((nf+2)/2) * (W/nf + 0.29)'
+ nrd='0.29 / W' nrs='0.29 / W' sa=0 sb=0 sd=0 mult=1 m=1
XM9_dummy_15 dummy_9 bias1 dummy_9 VCC sky130_fd_pr__pfet_01v8 L=15 W=5 nf=1 ad='int((nf+1)/2) * W/nf * 0.29'
+ as='int((nf+2)/2) * W/nf * 0.29' pd='2*int((nf+1)/2) * (W/nf + 0.29)' ps='2*int((nf+2)/2) * (W/nf + 0.29)'
+ nrd='0.29 / W' nrs='0.29 / W' sa=0 sb=0 sd=0 mult=1 m=1
XM9_dummy_16 dummy_9 bias1 dummy_9 VCC sky130_fd_pr__pfet_01v8 L=15 W=5 nf=1 ad='int((nf+1)/2) * W/nf * 0.29'
+ as='int((nf+2)/2) * W/nf * 0.29' pd='2*int((nf+1)/2) * (W/nf + 0.29)' ps='2*int((nf+2)/2) * (W/nf + 0.29)'
+ nrd='0.29 / W' nrs='0.29 / W' sa=0 sb=0 sd=0 mult=1 m=1
XM9_dummy_17 dummy_9 bias1 dummy_9 VCC sky130_fd_pr__pfet_01v8 L=15 W=5 nf=1 ad='int((nf+1)/2) * W/nf * 0.29'
+ as='int((nf+2)/2) * W/nf * 0.29' pd='2*int((nf+1)/2) * (W/nf + 0.29)' ps='2*int((nf+2)/2) * (W/nf + 0.29)'
+ nrd='0.29 / W' nrs='0.29 / W' sa=0 sb=0 sd=0 mult=1 m=1
XM9_dummy_18 dummy_9 bias1 dummy_9 VCC sky130_fd_pr__pfet_01v8 L=15 W=5 nf=1 ad='int((nf+1)/2) * W/nf * 0.29'
+ as='int((nf+2)/2) * W/nf * 0.29' pd='2*int((nf+1)/2) * (W/nf + 0.29)' ps='2*int((nf+2)/2) * (W/nf + 0.29)'
+ nrd='0.29 / W' nrs='0.29 / W' sa=0 sb=0 sd=0 mult=1 m=1
XM9_dummy_19 dummy_9 bias1 dummy_9 VCC sky130_fd_pr__pfet_01v8 L=15 W=5 nf=1 ad='int((nf+1)/2) * W/nf * 0.29'
+ as='int((nf+2)/2) * W/nf * 0.29' pd='2*int((nf+1)/2) * (W/nf + 0.29)' ps='2*int((nf+2)/2) * (W/nf + 0.29)'
+ nrd='0.29 / W' nrs='0.29 / W' sa=0 sb=0 sd=0 mult=1 m=1
XM9_dummy_20 dummy_9 bias1 dummy_9 VCC sky130_fd_pr__pfet_01v8 L=15 W=5 nf=1 ad='int((nf+1)/2) * W/nf * 0.29'
+ as='int((nf+2)/2) * W/nf * 0.29' pd='2*int((nf+1)/2) * (W/nf + 0.29)' ps='2*int((nf+2)/2) * (W/nf + 0.29)'
+ nrd='0.29 / W' nrs='0.29 / W' sa=0 sb=0 sd=0 mult=1 m=1
XM9_dummy_21 dummy_9 bias1 dummy_9 VCC sky130_fd_pr__pfet_01v8 L=15 W=5 nf=1 ad='int((nf+1)/2) * W/nf * 0.29'
+ as='int((nf+2)/2) * W/nf * 0.29' pd='2*int((nf+1)/2) * (W/nf + 0.29)' ps='2*int((nf+2)/2) * (W/nf + 0.29)'
+ nrd='0.29 / W' nrs='0.29 / W' sa=0 sb=0 sd=0 mult=1 m=1
XM9_dummy_22 dummy_9 bias1 dummy_9 VCC sky130_fd_pr__pfet_01v8 L=15 W=5 nf=1 ad='int((nf+1)/2) * W/nf * 0.29'
+ as='int((nf+2)/2) * W/nf * 0.29' pd='2*int((nf+1)/2) * (W/nf + 0.29)' ps='2*int((nf+2)/2) * (W/nf + 0.29)'
+ nrd='0.29 / W' nrs='0.29 / W' sa=0 sb=0 sd=0 mult=1 m=1
.ends

.GLOBAL GND
.end
